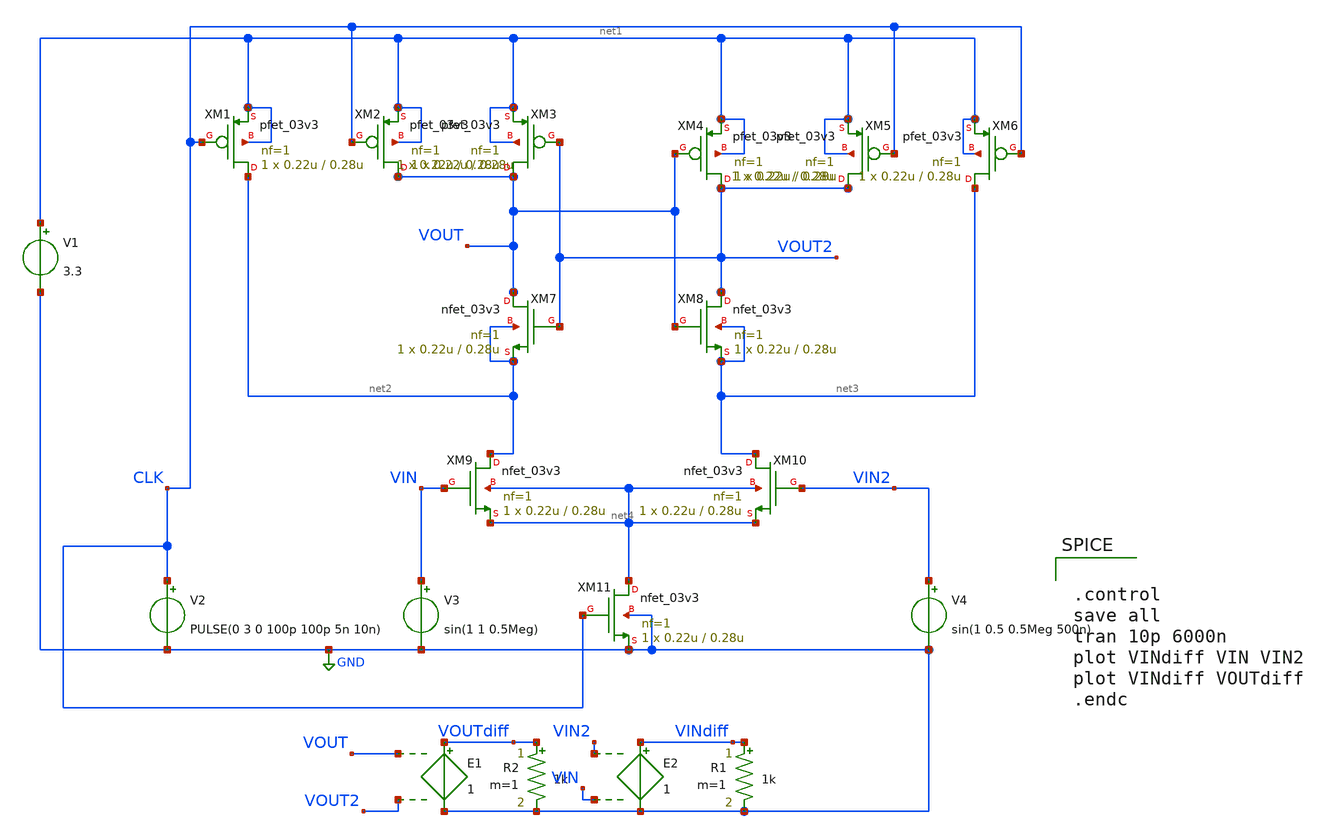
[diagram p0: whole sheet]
** sch_path: StrongARM.sch
**.subckt StrongARM
XM1 net2 CLK net1 net1 pfet_03v3 L=0.28u W=0.22u nf=1 ad='int((nf+1)/2) * W/nf * 0.18u' as='int((nf+2)/2) * W/nf * 0.18u'
+ pd='2*int((nf+1)/2) * (W/nf + 0.18u)' ps='2*int((nf+2)/2) * (W/nf + 0.18u)' nrd='0.18u / W' nrs='0.18u / W'
+ sa=0 sb=0 sd=0 m=1
XM2 VOUT CLK net1 net1 pfet_03v3 L=0.28u W=0.22u nf=1 ad='int((nf+1)/2) * W/nf * 0.18u' as='int((nf+2)/2) * W/nf * 0.18u'
+ pd='2*int((nf+1)/2) * (W/nf + 0.18u)' ps='2*int((nf+2)/2) * (W/nf + 0.18u)' nrd='0.18u / W' nrs='0.18u / W'
+ sa=0 sb=0 sd=0 m=1
XM3 VOUT VOUT2 net1 net1 pfet_03v3 L=0.28u W=0.22u nf=1 ad='int((nf+1)/2) * W/nf * 0.18u' as='int((nf+2)/2) * W/nf * 0.18u'
+ pd='2*int((nf+1)/2) * (W/nf + 0.18u)' ps='2*int((nf+2)/2) * (W/nf + 0.18u)' nrd='0.18u / W' nrs='0.18u / W'
+ sa=0 sb=0 sd=0 m=1
XM4 VOUT2 VOUT net1 net1 pfet_03v3 L=0.28u W=0.22u nf=1 ad='int((nf+1)/2) * W/nf * 0.18u' as='int((nf+2)/2) * W/nf * 0.18u'
+ pd='2*int((nf+1)/2) * (W/nf + 0.18u)' ps='2*int((nf+2)/2) * (W/nf + 0.18u)' nrd='0.18u / W' nrs='0.18u / W'
+ sa=0 sb=0 sd=0 m=1
XM5 VOUT2 CLK net1 net1 pfet_03v3 L=0.28u W=0.22u nf=1 ad='int((nf+1)/2) * W/nf * 0.18u' as='int((nf+2)/2) * W/nf * 0.18u'
+ pd='2*int((nf+1)/2) * (W/nf + 0.18u)' ps='2*int((nf+2)/2) * (W/nf + 0.18u)' nrd='0.18u / W' nrs='0.18u / W'
+ sa=0 sb=0 sd=0 m=1
XM6 net3 CLK net1 net1 pfet_03v3 L=0.28u W=0.22u nf=1 ad='int((nf+1)/2) * W/nf * 0.18u' as='int((nf+2)/2) * W/nf * 0.18u'
+ pd='2*int((nf+1)/2) * (W/nf + 0.18u)' ps='2*int((nf+2)/2) * (W/nf + 0.18u)' nrd='0.18u / W' nrs='0.18u / W'
+ sa=0 sb=0 sd=0 m=1
XM7 VOUT VOUT2 net2 net2 nfet_03v3 L=0.28u W=0.22u nf=1 ad='int((nf+1)/2) * W/nf * 0.18u' as='int((nf+2)/2) * W/nf * 0.18u'
+ pd='2*int((nf+1)/2) * (W/nf + 0.18u)' ps='2*int((nf+2)/2) * (W/nf + 0.18u)' nrd='0.18u / W' nrs='0.18u / W'
+ sa=0 sb=0 sd=0 m=1
XM8 VOUT2 VOUT net3 net3 nfet_03v3 L=0.28u W=0.22u nf=1 ad='int((nf+1)/2) * W/nf * 0.18u' as='int((nf+2)/2) * W/nf * 0.18u'
+ pd='2*int((nf+1)/2) * (W/nf + 0.18u)' ps='2*int((nf+2)/2) * (W/nf + 0.18u)' nrd='0.18u / W' nrs='0.18u / W'
+ sa=0 sb=0 sd=0 m=1
XM9 net2 VIN net4 net4 nfet_03v3 L=0.28u W=0.22u nf=1 ad='int((nf+1)/2) * W/nf * 0.18u' as='int((nf+2)/2) * W/nf * 0.18u'
+ pd='2*int((nf+1)/2) * (W/nf + 0.18u)' ps='2*int((nf+2)/2) * (W/nf + 0.18u)' nrd='0.18u / W' nrs='0.18u / W'
+ sa=0 sb=0 sd=0 m=1
XM10 net3 VIN2 net4 net4 nfet_03v3 L=0.28u W=0.22u nf=1 ad='int((nf+1)/2) * W/nf * 0.18u' as='int((nf+2)/2) * W/nf * 0.18u'
+ pd='2*int((nf+1)/2) * (W/nf + 0.18u)' ps='2*int((nf+2)/2) * (W/nf + 0.18u)' nrd='0.18u / W' nrs='0.18u / W'
+ sa=0 sb=0 sd=0 m=1
XM11 net4 CLK GND GND nfet_03v3 L=0.28u W=0.22u nf=1 ad='int((nf+1)/2) * W/nf * 0.18u' as='int((nf+2)/2) * W/nf * 0.18u'
+ pd='2*int((nf+1)/2) * (W/nf + 0.18u)' ps='2*int((nf+2)/2) * (W/nf + 0.18u)' nrd='0.18u / W' nrs='0.18u / W'
+ sa=0 sb=0 sd=0 m=1
V1 net1 GND 3.3
V2 CLK GND PULSE(0 3 0 100p 100p 5n 10n)
V3 VIN GND sin(1 1 0.5Meg)
V4 VIN2 GND sin(1 0.5 0.5Meg 500n)
R2 VOUTdiff GND 1k m=1
E1 VOUTdiff GND VOUT VOUT2 1
R1 VINdiff GND 1k m=1
E2 VINdiff GND VIN2 VIN 1
**** begin user architecture code


.control
save all
tran 10p 6000n
plot VINdiff VIN VIN2
plot VINdiff VOUTdiff
.endc


.include /foss/pdks/gf180mcuC/libs.tech/ngspice/design.ngspice
.lib /foss/pdks/gf180mcuC/libs.tech/ngspice/sm141064.ngspice typical

**** end user architecture code
**.ends
.GLOBAL GND
.end
